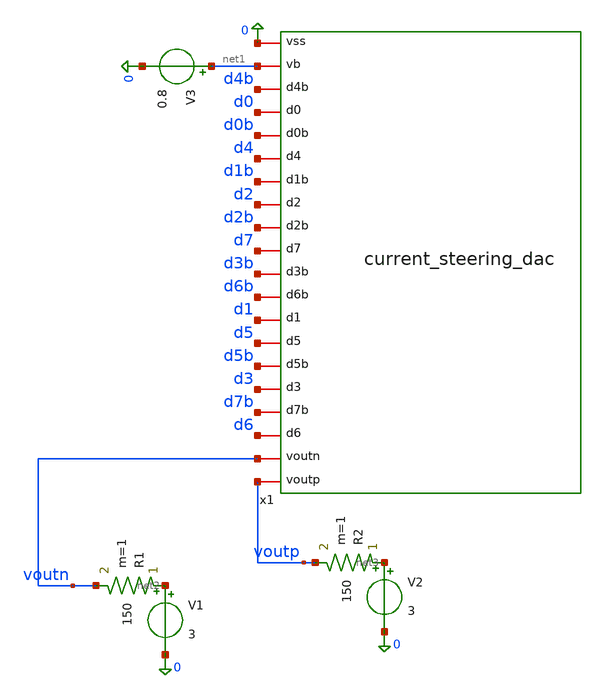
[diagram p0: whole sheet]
** sch_path: analog/dac/dac_sim.sch
**.subckt dac_sim
R1 net2 voutn 150 m=1
V1 net2 0 3
R2 net3 voutp 150 m=1
V2 net3 0 3
V3 net1 0 0.8
x1 voutp voutn d6 d7b d3 d5b d5 d1 d6b d3b d7 d2b d2 d1b d4 d0b d0 d4b net1 0 current_steering_dac
**** begin user architecture code



.include /foss/pdks/gf180mcuD/libs.tech/ngspice/design.ngspice
.lib /foss/pdks/gf180mcuD/libs.tech/ngspice/sm141064.ngspice typical
.lib /foss/pdks/gf180mcuD/libs.tech/ngspice/sm141064.ngspice mimcap_typical

** Eight-bit binary input stimulus
** Each input code is held for 125 ns
** The complete 0-to-255 sweep takes 32 us

VD0  D0  0 PULSE(0   3.3 125n 1n 1n 125n 250n)
VD0B D0b 0 PULSE(3.3 0   125n 1n 1n 125n 250n)

VD1  D1  0 PULSE(0   3.3 250n 1n 1n 250n 500n)
VD1B D1b 0 PULSE(3.3 0   250n 1n 1n 250n 500n)

VD2  D2  0 PULSE(0   3.3 500n 1n 1n 500n 1u)
VD2B D2b 0 PULSE(3.3 0   500n 1n 1n 500n 1u)

VD3  D3  0 PULSE(0   3.3 1u 1n 1n 1u 2u)
VD3B D3b 0 PULSE(3.3 0   1u 1n 1n 1u 2u)

VD4  D4  0 PULSE(0   3.3 2u 1n 1n 2u 4u)
VD4B D4b 0 PULSE(3.3 0   2u 1n 1n 2u 4u)

VD5  D5  0 PULSE(0   3.3 4u 1n 1n 4u 8u)
VD5B D5b 0 PULSE(3.3 0   4u 1n 1n 4u 8u)

VD6  D6  0 PULSE(0   3.3 8u 1n 1n 8u 16u)
VD6B D6b 0 PULSE(3.3 0   8u 1n 1n 8u 16u)

VD7  D7  0 PULSE(0   3.3 16u 1n 1n 16u 32u)
VD7B D7b 0 PULSE(3.3 0   16u 1n 1n 16u 32u)

.control

tran 1n 32u

** Display the binary inputs
**plot v(D0) v(D1) v(D2) v(D3)
**plot v(D4) v(D5) v(D6) v(D7)

plot v(voutp)
plot v(voutp)-v(voutn)


set wr_singlescale
set wr_vecnames
wrdata dac_output.txt v(voutp) v(voutn) v(voutp)-v(voutn)


.endc



**** end user architecture code
**.ends

* expanding   symbol:  current_steering_dac.sym # of pins=20
** sym_path: analog/dac/current_steering_dac.sym
** sch_path: analog/dac/current_steering_dac.sch
.subckt current_steering_dac voutp voutn d6 d7b d3 d5b d5 d1 d6b d3b d7 d2b d2 d1b d4 d0b d0 d4b vb
+ vss
*.iopin voutp
*.iopin voutn
*.iopin d7b
*.iopin d7
*.iopin d6b
*.iopin d6
*.iopin d5b
*.iopin d5
*.iopin d4b
*.iopin d4
*.iopin d3b
*.iopin d3
*.iopin d2b
*.iopin d2
*.iopin d1b
*.iopin d1
*.iopin d0b
*.iopin d0
*.iopin vb
*.iopin vss
XM1 voutp d0 net1 vss nfet_03v3 L=0.28u W=0.56u nf=1 ad='int((nf+1)/2) * W/nf * 0.18u' as='int((nf+2)/2) * W/nf * 0.18u'
+ pd='2*int((nf+1)/2) * (W/nf + 0.18u)' ps='2*int((nf+2)/2) * (W/nf + 0.18u)' nrd='0.18u / W' nrs='0.18u / W'
+ sa=0 sb=0 sd=0 m=1
XM7 net1 vb vss vss nfet_03v3 L=1u W=2u nf=1 ad='int((nf+1)/2) * W/nf * 0.18u' as='int((nf+2)/2) * W/nf * 0.18u'
+ pd='2*int((nf+1)/2) * (W/nf + 0.18u)' ps='2*int((nf+2)/2) * (W/nf + 0.18u)' nrd='0.18u / W' nrs='0.18u / W'
+ sa=0 sb=0 sd=0 m=1
XM5 net2 vb vss vss nfet_03v3 L=1u W=4u nf=1 ad='int((nf+1)/2) * W/nf * 0.18u' as='int((nf+2)/2) * W/nf * 0.18u'
+ pd='2*int((nf+1)/2) * (W/nf + 0.18u)' ps='2*int((nf+2)/2) * (W/nf + 0.18u)' nrd='0.18u / W' nrs='0.18u / W'
+ sa=0 sb=0 sd=0 m=1
XM9 net3 vb vss vss nfet_03v3 L=1u W=8u nf=1 ad='int((nf+1)/2) * W/nf * 0.18u' as='int((nf+2)/2) * W/nf * 0.18u'
+ pd='2*int((nf+1)/2) * (W/nf + 0.18u)' ps='2*int((nf+2)/2) * (W/nf + 0.18u)' nrd='0.18u / W' nrs='0.18u / W'
+ sa=0 sb=0 sd=0 m=1
XM12 net4 vb vss vss nfet_03v3 L=1u W=16u nf=1 ad='int((nf+1)/2) * W/nf * 0.18u' as='int((nf+2)/2) * W/nf * 0.18u'
+ pd='2*int((nf+1)/2) * (W/nf + 0.18u)' ps='2*int((nf+2)/2) * (W/nf + 0.18u)' nrd='0.18u / W' nrs='0.18u / W'
+ sa=0 sb=0 sd=0 m=1
XM13 voutp d4 net5 vss nfet_03v3 L=0.28u W=8.96u nf=1 ad='int((nf+1)/2) * W/nf * 0.18u' as='int((nf+2)/2) * W/nf * 0.18u'
+ pd='2*int((nf+1)/2) * (W/nf + 0.18u)' ps='2*int((nf+2)/2) * (W/nf + 0.18u)' nrd='0.18u / W' nrs='0.18u / W'
+ sa=0 sb=0 sd=0 m=1
XM15 net5 vb vss vss nfet_03v3 L=1u W=32u nf=1 ad='int((nf+1)/2) * W/nf * 0.18u' as='int((nf+2)/2) * W/nf * 0.18u'
+ pd='2*int((nf+1)/2) * (W/nf + 0.18u)' ps='2*int((nf+2)/2) * (W/nf + 0.18u)' nrd='0.18u / W' nrs='0.18u / W'
+ sa=0 sb=0 sd=0 m=1
XM16 voutp d5 net6 vss nfet_03v3 L=0.28u W=17.92u nf=1 ad='int((nf+1)/2) * W/nf * 0.18u' as='int((nf+2)/2) * W/nf * 0.18u'
+ pd='2*int((nf+1)/2) * (W/nf + 0.18u)' ps='2*int((nf+2)/2) * (W/nf + 0.18u)' nrd='0.18u / W' nrs='0.18u / W'
+ sa=0 sb=0 sd=0 m=1
XM18 net6 vb vss vss nfet_03v3 L=1u W=64u nf=1 ad='int((nf+1)/2) * W/nf * 0.18u' as='int((nf+2)/2) * W/nf * 0.18u'
+ pd='2*int((nf+1)/2) * (W/nf + 0.18u)' ps='2*int((nf+2)/2) * (W/nf + 0.18u)' nrd='0.18u / W' nrs='0.18u / W'
+ sa=0 sb=0 sd=0 m=1
XM19 voutp d6 net7 vss nfet_03v3 L=0.28u W=35.84u nf=1 ad='int((nf+1)/2) * W/nf * 0.18u' as='int((nf+2)/2) * W/nf * 0.18u'
+ pd='2*int((nf+1)/2) * (W/nf + 0.18u)' ps='2*int((nf+2)/2) * (W/nf + 0.18u)' nrd='0.18u / W' nrs='0.18u / W'
+ sa=0 sb=0 sd=0 m=1
XM21 net7 vb vss vss nfet_03v3 L=1u W=64u nf=1 ad='int((nf+1)/2) * W/nf * 0.18u' as='int((nf+2)/2) * W/nf * 0.18u'
+ pd='2*int((nf+1)/2) * (W/nf + 0.18u)' ps='2*int((nf+2)/2) * (W/nf + 0.18u)' nrd='0.18u / W' nrs='0.18u / W'
+ sa=0 sb=0 sd=0 m=2
XM23 voutp d7 net8 vss nfet_03v3 L=0.28u W=35.84u nf=1 ad='int((nf+1)/2) * W/nf * 0.18u' as='int((nf+2)/2) * W/nf * 0.18u'
+ pd='2*int((nf+1)/2) * (W/nf + 0.18u)' ps='2*int((nf+2)/2) * (W/nf + 0.18u)' nrd='0.18u / W' nrs='0.18u / W'
+ sa=0 sb=0 sd=0 m=2
XM25 net8 vb vss vss nfet_03v3 L=1u W=64u nf=1 ad='int((nf+1)/2) * W/nf * 0.18u' as='int((nf+2)/2) * W/nf * 0.18u'
+ pd='2*int((nf+1)/2) * (W/nf + 0.18u)' ps='2*int((nf+2)/2) * (W/nf + 0.18u)' nrd='0.18u / W' nrs='0.18u / W'
+ sa=0 sb=0 sd=0 m=4
XM3 voutp d1 net2 vss nfet_03v3 L=0.28u W=1.12u nf=1 ad='int((nf+1)/2) * W/nf * 0.18u' as='int((nf+2)/2) * W/nf * 0.18u'
+ pd='2*int((nf+1)/2) * (W/nf + 0.18u)' ps='2*int((nf+2)/2) * (W/nf + 0.18u)' nrd='0.18u / W' nrs='0.18u / W'
+ sa=0 sb=0 sd=0 m=1
XM6 voutp d2 net3 vss nfet_03v3 L=0.28u W=2.24u nf=1 ad='int((nf+1)/2) * W/nf * 0.18u' as='int((nf+2)/2) * W/nf * 0.18u'
+ pd='2*int((nf+1)/2) * (W/nf + 0.18u)' ps='2*int((nf+2)/2) * (W/nf + 0.18u)' nrd='0.18u / W' nrs='0.18u / W'
+ sa=0 sb=0 sd=0 m=1
XM10 voutp d3 net4 vss nfet_03v3 L=0.28u W=4.48u nf=1 ad='int((nf+1)/2) * W/nf * 0.18u' as='int((nf+2)/2) * W/nf * 0.18u'
+ pd='2*int((nf+1)/2) * (W/nf + 0.18u)' ps='2*int((nf+2)/2) * (W/nf + 0.18u)' nrd='0.18u / W' nrs='0.18u / W'
+ sa=0 sb=0 sd=0 m=1
XM2 voutn d0b net1 vss nfet_03v3 L=0.28u W=0.56u nf=1 ad='int((nf+1)/2) * W/nf * 0.18u' as='int((nf+2)/2) * W/nf * 0.18u'
+ pd='2*int((nf+1)/2) * (W/nf + 0.18u)' ps='2*int((nf+2)/2) * (W/nf + 0.18u)' nrd='0.18u / W' nrs='0.18u / W'
+ sa=0 sb=0 sd=0 m=1
XM4 voutn d1b net2 vss nfet_03v3 L=0.28u W=1.12u nf=1 ad='int((nf+1)/2) * W/nf * 0.18u' as='int((nf+2)/2) * W/nf * 0.18u'
+ pd='2*int((nf+1)/2) * (W/nf + 0.18u)' ps='2*int((nf+2)/2) * (W/nf + 0.18u)' nrd='0.18u / W' nrs='0.18u / W'
+ sa=0 sb=0 sd=0 m=1
XM8 voutn d2b net3 vss nfet_03v3 L=0.28u W=2.24u nf=1 ad='int((nf+1)/2) * W/nf * 0.18u' as='int((nf+2)/2) * W/nf * 0.18u'
+ pd='2*int((nf+1)/2) * (W/nf + 0.18u)' ps='2*int((nf+2)/2) * (W/nf + 0.18u)' nrd='0.18u / W' nrs='0.18u / W'
+ sa=0 sb=0 sd=0 m=1
XM11 voutn d3b net4 vss nfet_03v3 L=0.28u W=4.48u nf=1 ad='int((nf+1)/2) * W/nf * 0.18u' as='int((nf+2)/2) * W/nf * 0.18u'
+ pd='2*int((nf+1)/2) * (W/nf + 0.18u)' ps='2*int((nf+2)/2) * (W/nf + 0.18u)' nrd='0.18u / W' nrs='0.18u / W'
+ sa=0 sb=0 sd=0 m=1
XM14 voutn d4b net5 vss nfet_03v3 L=0.28u W=8.96u nf=1 ad='int((nf+1)/2) * W/nf * 0.18u' as='int((nf+2)/2) * W/nf * 0.18u'
+ pd='2*int((nf+1)/2) * (W/nf + 0.18u)' ps='2*int((nf+2)/2) * (W/nf + 0.18u)' nrd='0.18u / W' nrs='0.18u / W'
+ sa=0 sb=0 sd=0 m=1
XM17 voutn d5b net6 vss nfet_03v3 L=0.28u W=17.92u nf=1 ad='int((nf+1)/2) * W/nf * 0.18u' as='int((nf+2)/2) * W/nf * 0.18u'
+ pd='2*int((nf+1)/2) * (W/nf + 0.18u)' ps='2*int((nf+2)/2) * (W/nf + 0.18u)' nrd='0.18u / W' nrs='0.18u / W'
+ sa=0 sb=0 sd=0 m=1
XM20 voutn d6b net7 vss nfet_03v3 L=0.28u W=35.84u nf=1 ad='int((nf+1)/2) * W/nf * 0.18u' as='int((nf+2)/2) * W/nf * 0.18u'
+ pd='2*int((nf+1)/2) * (W/nf + 0.18u)' ps='2*int((nf+2)/2) * (W/nf + 0.18u)' nrd='0.18u / W' nrs='0.18u / W'
+ sa=0 sb=0 sd=0 m=1
XM22 voutn d7b net8 vss nfet_03v3 L=0.28u W=35.84u nf=1 ad='int((nf+1)/2) * W/nf * 0.18u' as='int((nf+2)/2) * W/nf * 0.18u'
+ pd='2*int((nf+1)/2) * (W/nf + 0.18u)' ps='2*int((nf+2)/2) * (W/nf + 0.18u)' nrd='0.18u / W' nrs='0.18u / W'
+ sa=0 sb=0 sd=0 m=2
.ends

.end
